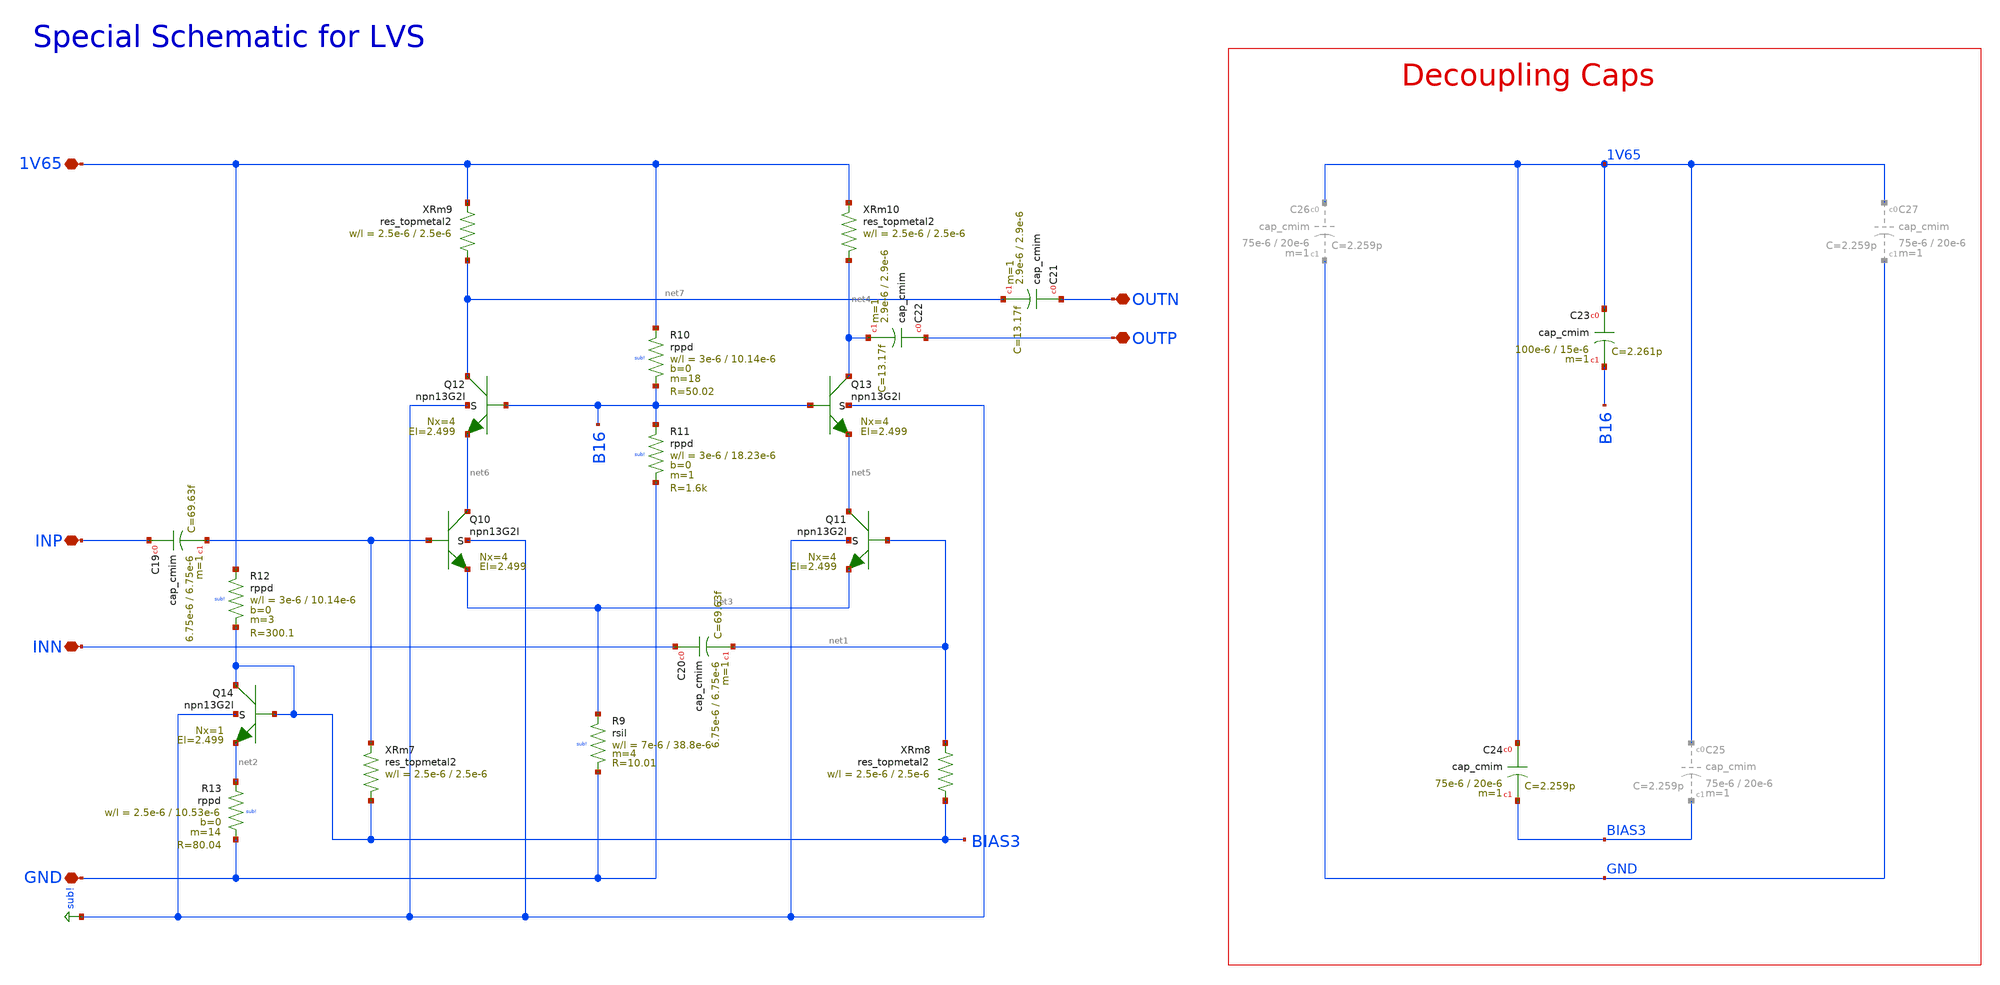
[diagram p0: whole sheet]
** sch_path: mWATTBAT/design_data/lvs/MULT_50GD_150GD_LVS.sch
**.subckt MULT_50GD_150GD_LVS 1V65 GND OUTN OUTP INP INN
*.iopin 1V65
*.iopin GND
*.iopin OUTN
*.iopin OUTP
*.iopin INP
*.iopin INN
XQ10 net6 INP net3 sub! npn13G2l Nx=4 El=2.499 mm_ok=1
XQ11 net5 net1 net3 sub! npn13G2l Nx=4 El=2.499 mm_ok=1
XQ14 BIAS3 BIAS3 net2 sub! npn13G2l Nx=1 El=2.499 mm_ok=1
XQ12 net7 B16 net6 sub! npn13G2l Nx=4 El=2.499 mm_ok=1
XQ13 net4 B16 net5 sub! npn13G2l Nx=4 El=2.499 mm_ok=1
XC21 OUTN net7 cap_cmim w=2.9e-6 l=2.9e-6 m=1 mm_ok=1
XC22 OUTP net4 cap_cmim w=2.9e-6 l=2.9e-6 m=1 mm_ok=1
XC20 INN net1 cap_cmim w=6.75e-6 l=6.75e-6 m=1 mm_ok=1
XC24 1V65 BIAS3 cap_cmim w=75e-6 l=20e-6 m=1 mm_ok=1
XC23 1V65 B16 cap_cmim w=100e-6 l=15e-6 m=1 mm_ok=1
XR10 1V65 B16 sub! rppd w=3e-6 l=10.14e-6 m=18 b=0 mm_ok=1
XR11 B16 GND sub! rppd w=3e-6 l=18.23e-6 m=1 b=0 mm_ok=1
XR13 net2 GND sub! rppd w=2.5e-6 l=10.53e-6 m=14 b=0 mm_ok=1
XR12 1V65 BIAS3 sub! rppd w=3e-6 l=10.14e-6 m=3 b=0 mm_ok=1
XR9 net3 GND sub! rsil w=7e-6 l=38.8e-6 m=4 mm_ok=1
XRm7 BIAS3 INP res_topmetal2 w=2.5e-6 l=2.5e-6
XRm8 BIAS3 net1 res_topmetal2 w=2.5e-6 l=2.5e-6
XRm9 net7 1V65 res_topmetal2 w=2.5e-6 l=2.5e-6
XRm10 net4 1V65 res_topmetal2 w=2.5e-6 l=2.5e-6
**.ends
.GLOBAL sub!
.end
